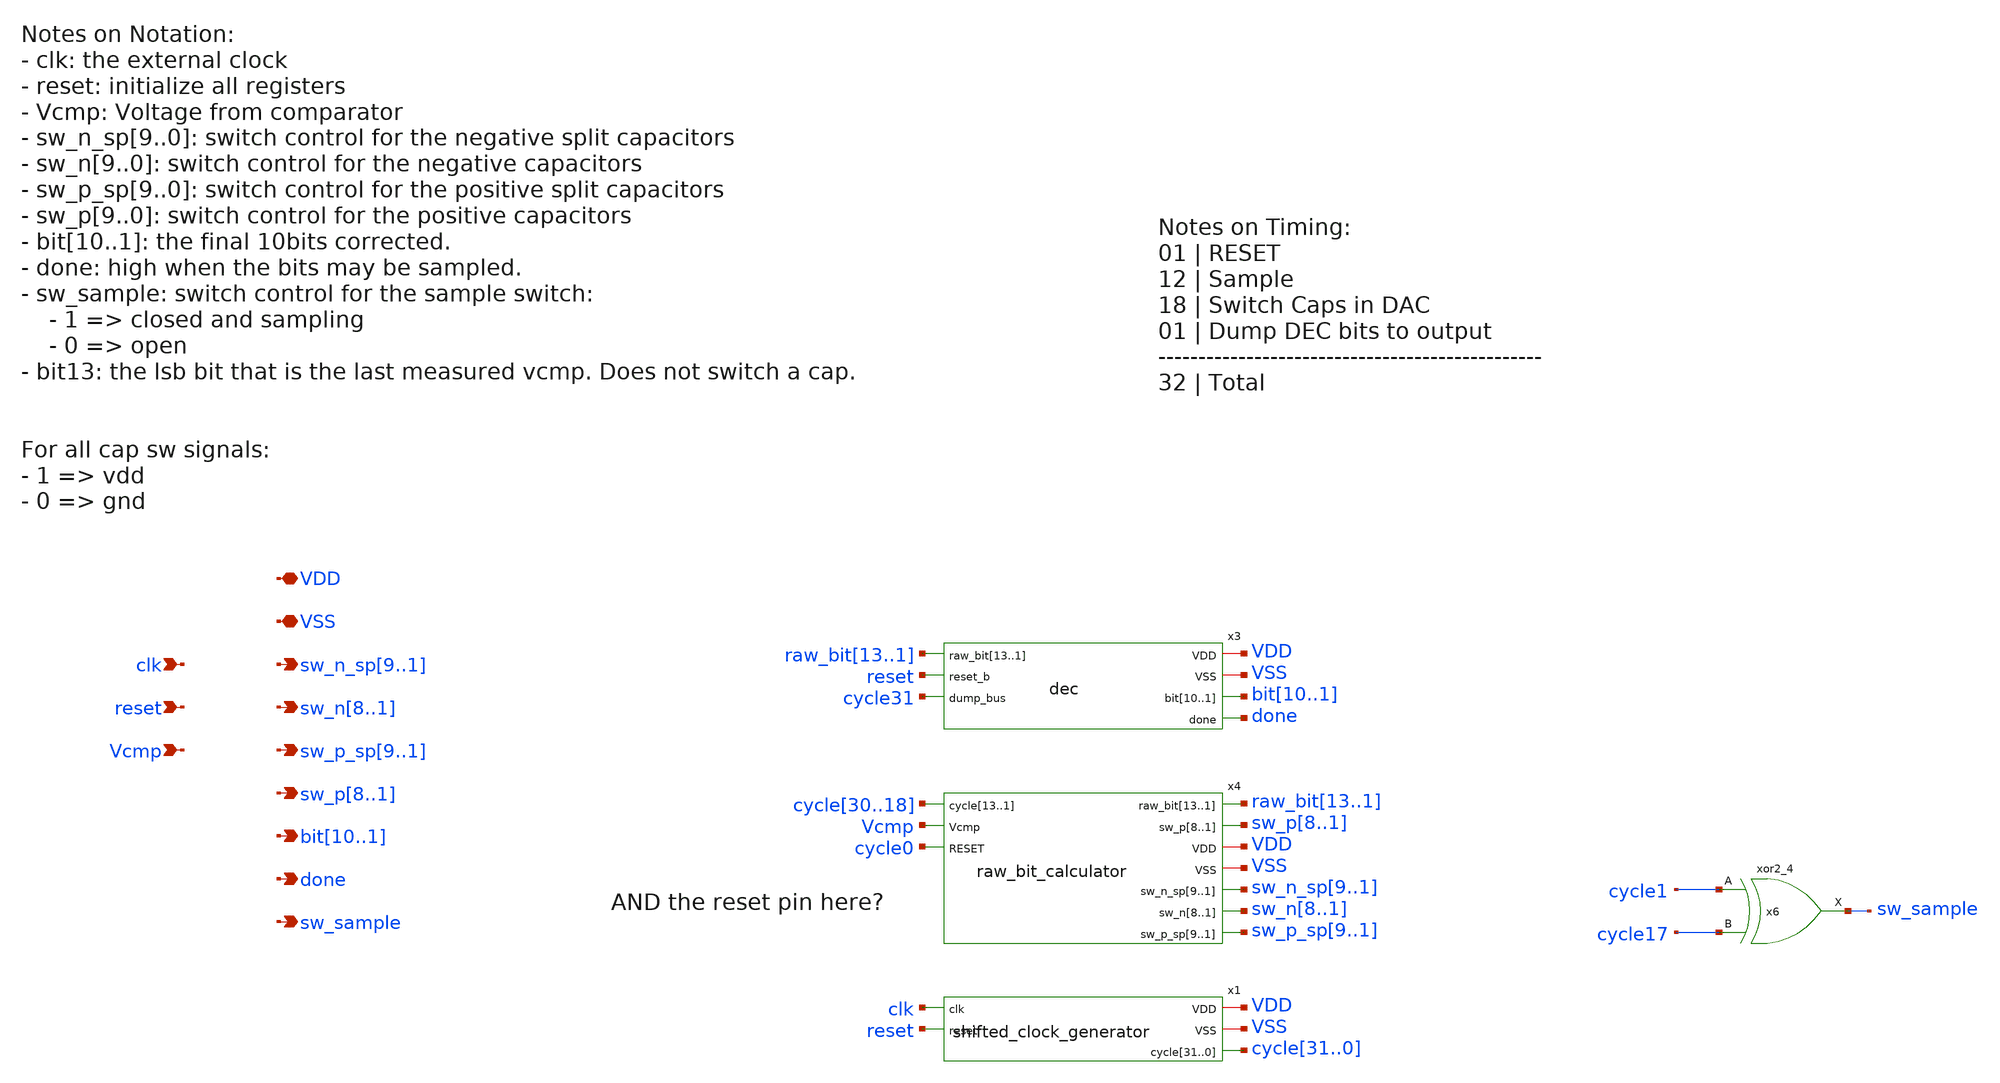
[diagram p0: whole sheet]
** sch_path: xschem/src/controller/controller.sch
**.subckt controller clk
*+ sw_n_sp9,sw_n_sp8,sw_n_sp7,sw_n_sp6,sw_n_sp5,sw_n_sp4,sw_n_sp3,sw_n_sp2,sw_n_sp1 VSS VDD reset Vcmp sw_n8,sw_n7,sw_n6,sw_n5,sw_n4,sw_n3,sw_n2,sw_n1
*+ sw_p_sp9,sw_p_sp8,sw_p_sp7,sw_p_sp6,sw_p_sp5,sw_p_sp4,sw_p_sp3,sw_p_sp2,sw_p_sp1 sw_p8,sw_p7,sw_p6,sw_p5,sw_p4,sw_p3,sw_p2,sw_p1 bit10,bit9,bit8,bit7,bit6,bit5,bit4,bit3,bit2,bit1
*+ done sw_sample
*.ipin clk
*.opin sw_n_sp9,sw_n_sp8,sw_n_sp7,sw_n_sp6,sw_n_sp5,sw_n_sp4,sw_n_sp3,sw_n_sp2,sw_n_sp1
*.iopin VSS
*.iopin VDD
*.ipin reset
*.ipin Vcmp
*.opin sw_n8,sw_n7,sw_n6,sw_n5,sw_n4,sw_n3,sw_n2,sw_n1
*.opin sw_p_sp9,sw_p_sp8,sw_p_sp7,sw_p_sp6,sw_p_sp5,sw_p_sp4,sw_p_sp3,sw_p_sp2,sw_p_sp1
*.opin sw_p8,sw_p7,sw_p6,sw_p5,sw_p4,sw_p3,sw_p2,sw_p1
*.opin bit10,bit9,bit8,bit7,bit6,bit5,bit4,bit3,bit2,bit1
*.opin done
*.opin sw_sample
x3 VDD raw_bit13 raw_bit12 raw_bit11 raw_bit10 raw_bit9 raw_bit8 raw_bit7 raw_bit6 raw_bit5 raw_bit4
+ raw_bit3 raw_bit2 raw_bit1 VSS reset bit10 bit9 bit8 bit7 bit6 bit5 bit4 bit3 bit2 bit1 done cycle31 dec
x4 raw_bit13 raw_bit12 raw_bit11 raw_bit10 raw_bit9 raw_bit8 raw_bit7 raw_bit6 raw_bit5 raw_bit4
+ raw_bit3 raw_bit2 raw_bit1 cycle30 cycle29 cycle28 cycle27 cycle26 cycle25 cycle24 cycle23 cycle22 cycle21
+ cycle20 cycle19 cycle18 sw_p8 sw_p7 sw_p6 sw_p5 sw_p4 sw_p3 sw_p2 sw_p1 Vcmp cycle0 VDD VSS sw_n_sp9
+ sw_n_sp8 sw_n_sp7 sw_n_sp6 sw_n_sp5 sw_n_sp4 sw_n_sp3 sw_n_sp2 sw_n_sp1 sw_n8 sw_n7 sw_n6 sw_n5 sw_n4 sw_n3
+ sw_n2 sw_n1 sw_p_sp9 sw_p_sp8 sw_p_sp7 sw_p_sp6 sw_p_sp5 sw_p_sp4 sw_p_sp3 sw_p_sp2 sw_p_sp1
+ raw_bit_calculator
x1 clk VDD VSS reset cycle31 cycle30 cycle29 cycle28 cycle27 cycle26 cycle25 cycle24 cycle23 cycle22
+ cycle21 cycle20 cycle19 cycle18 cycle17 cycle16 cycle15 cycle14 cycle13 cycle12 cycle11 cycle10 cycle9
+ cycle8 cycle7 cycle6 cycle5 cycle4 cycle3 cycle2 cycle1 cycle0 shifted_clock_generator
x6 cycle1 cycle17 VSS VSS VDD VDD sw_sample sky130_fd_sc_hd__xor2_4
**.ends
.end
